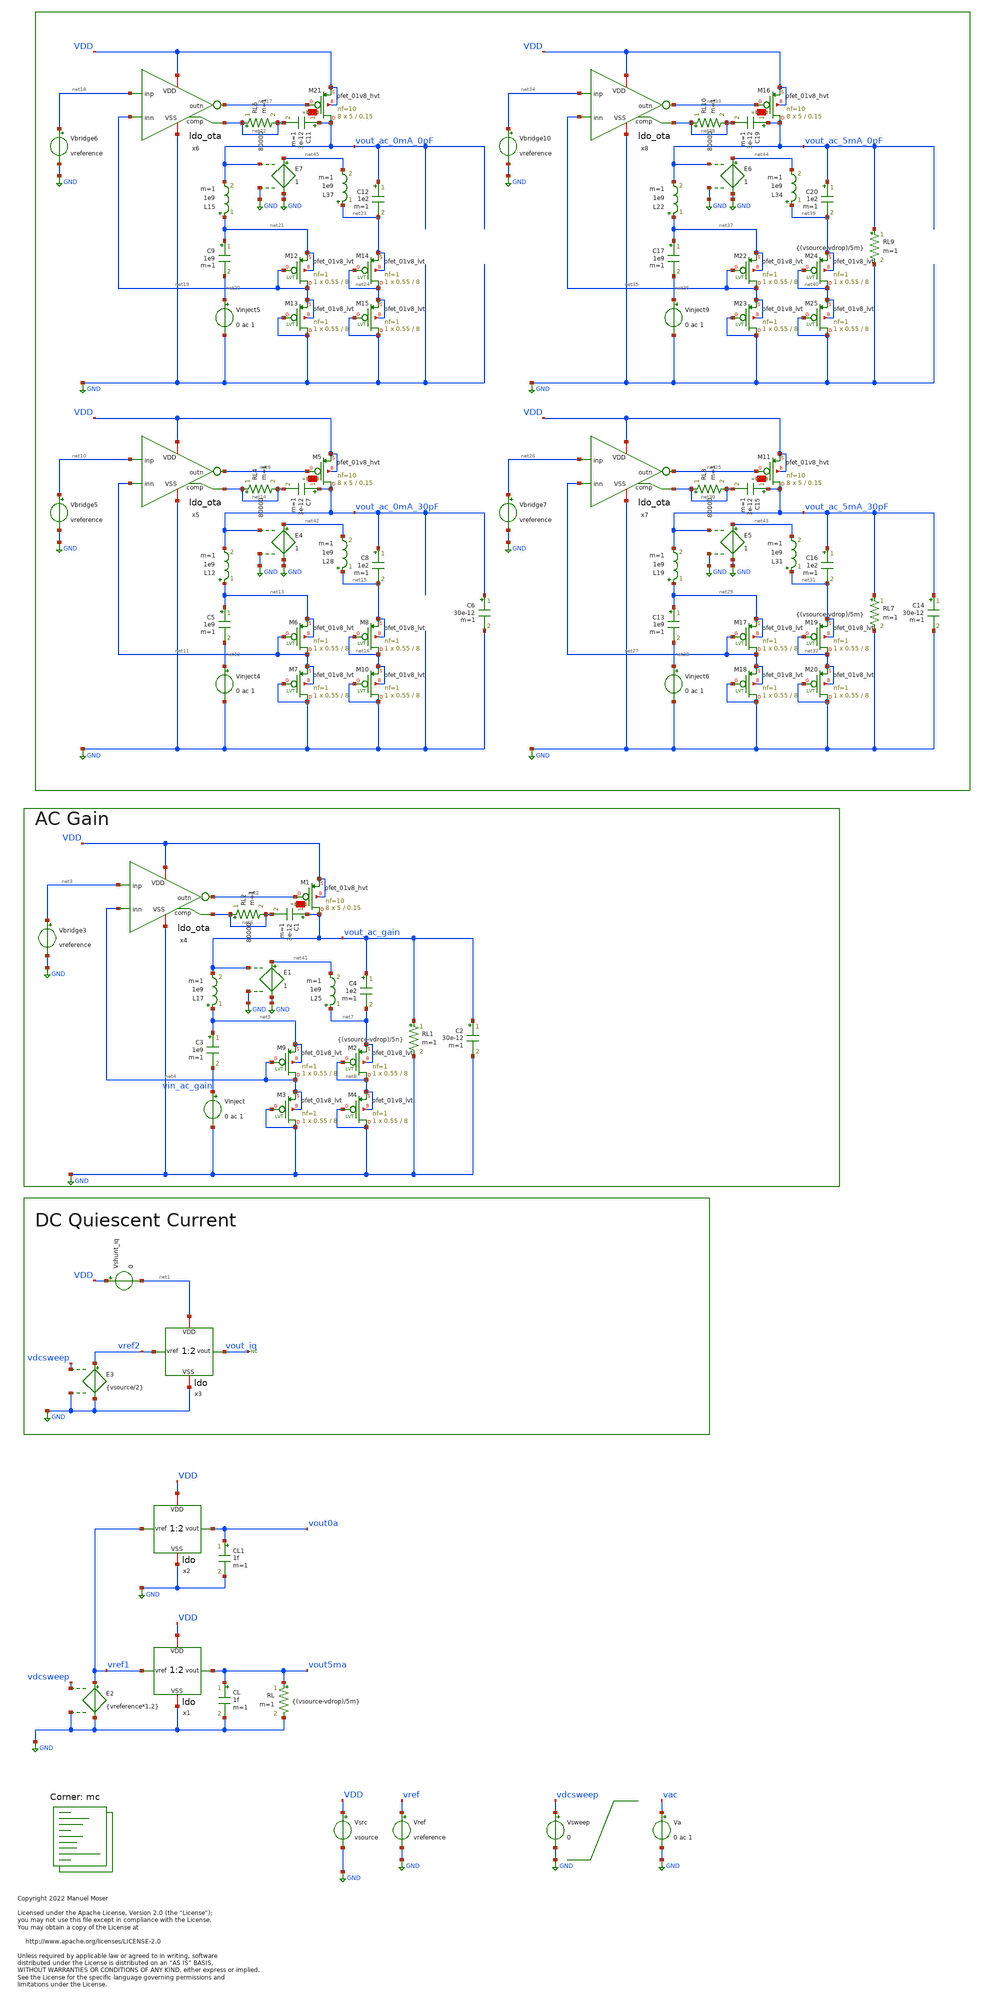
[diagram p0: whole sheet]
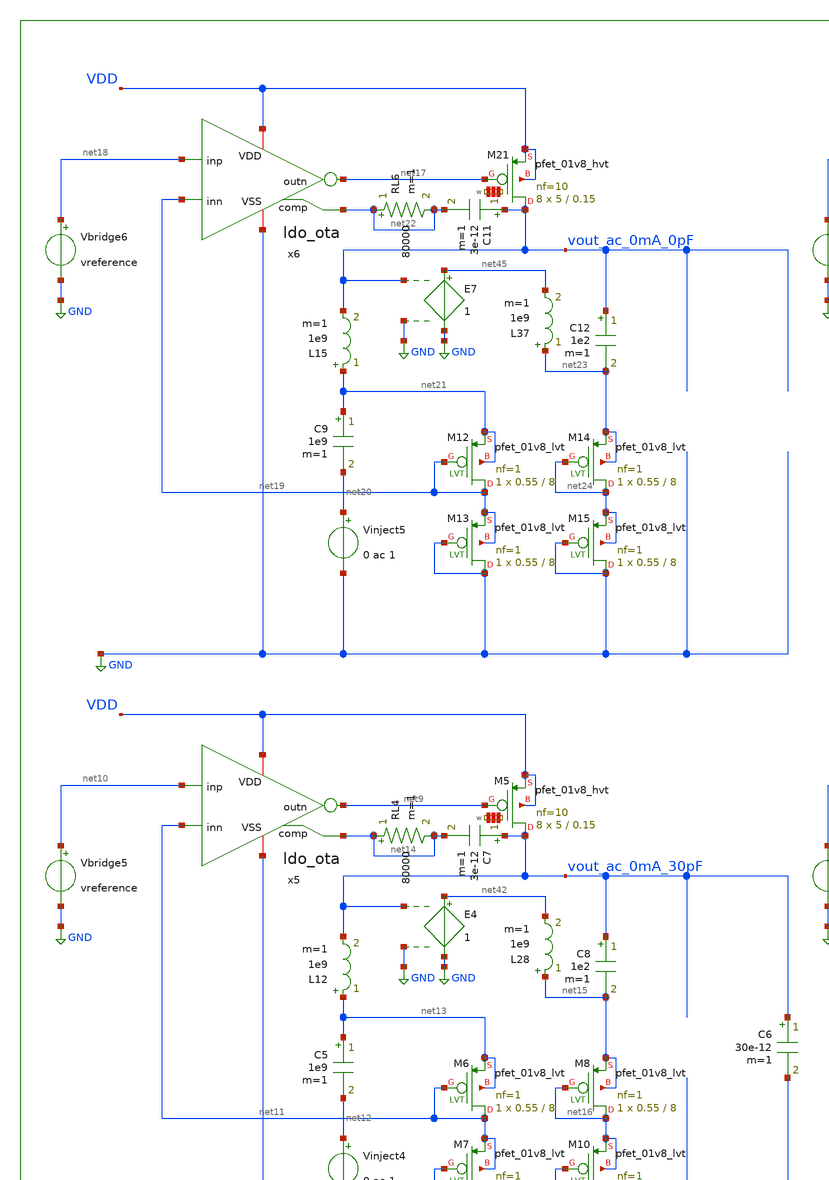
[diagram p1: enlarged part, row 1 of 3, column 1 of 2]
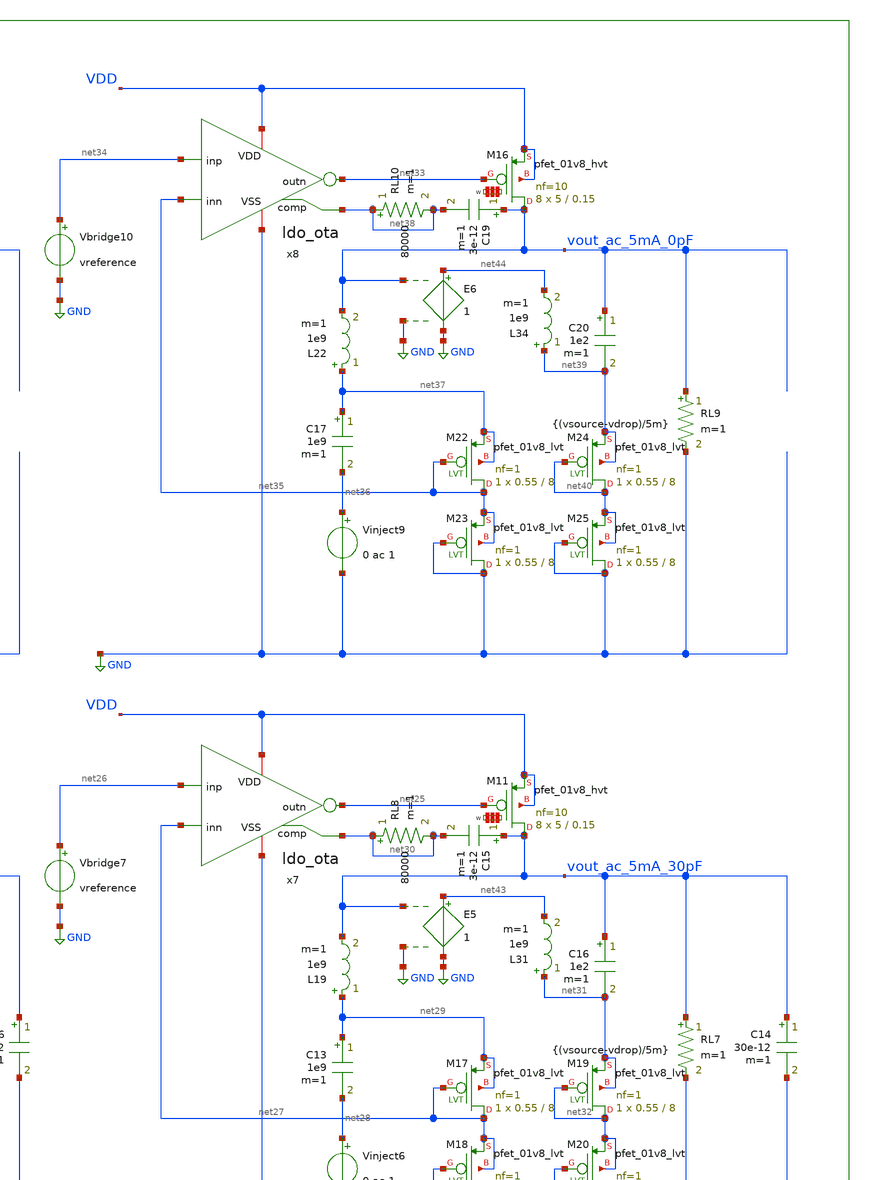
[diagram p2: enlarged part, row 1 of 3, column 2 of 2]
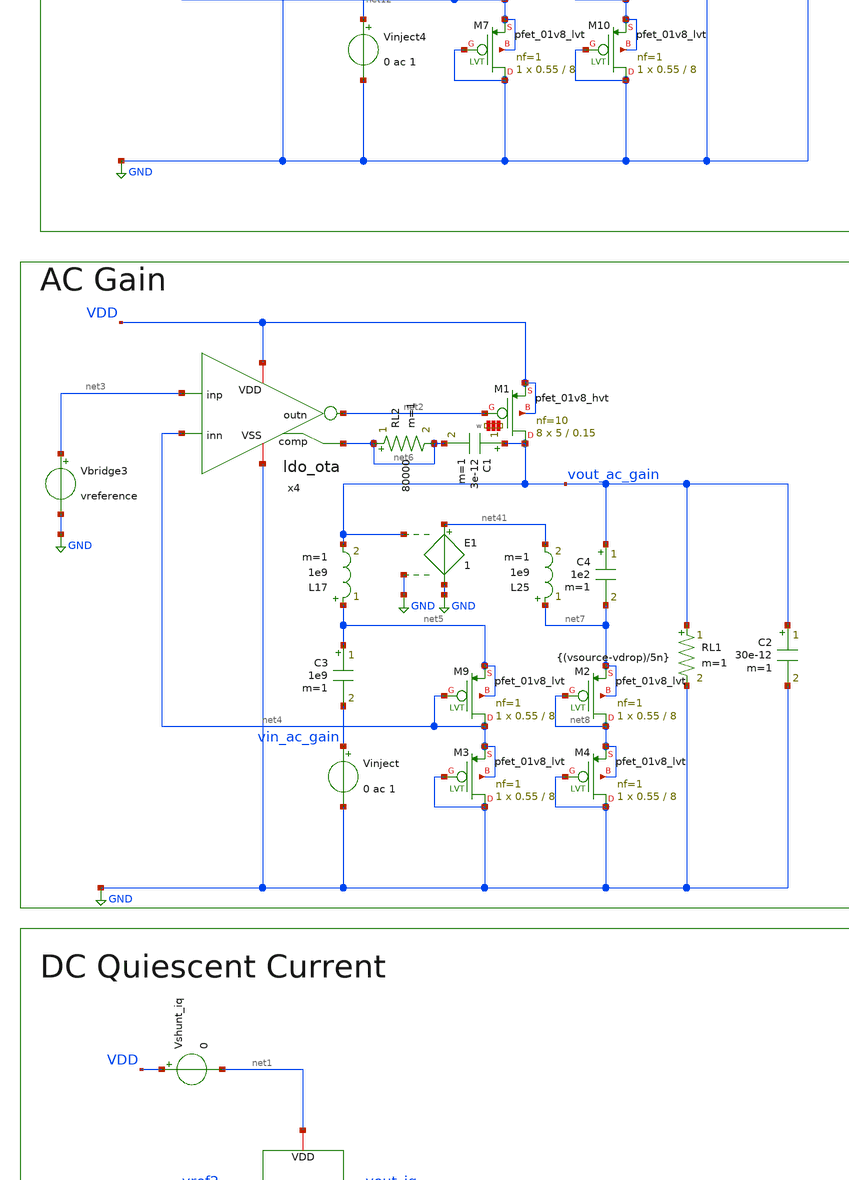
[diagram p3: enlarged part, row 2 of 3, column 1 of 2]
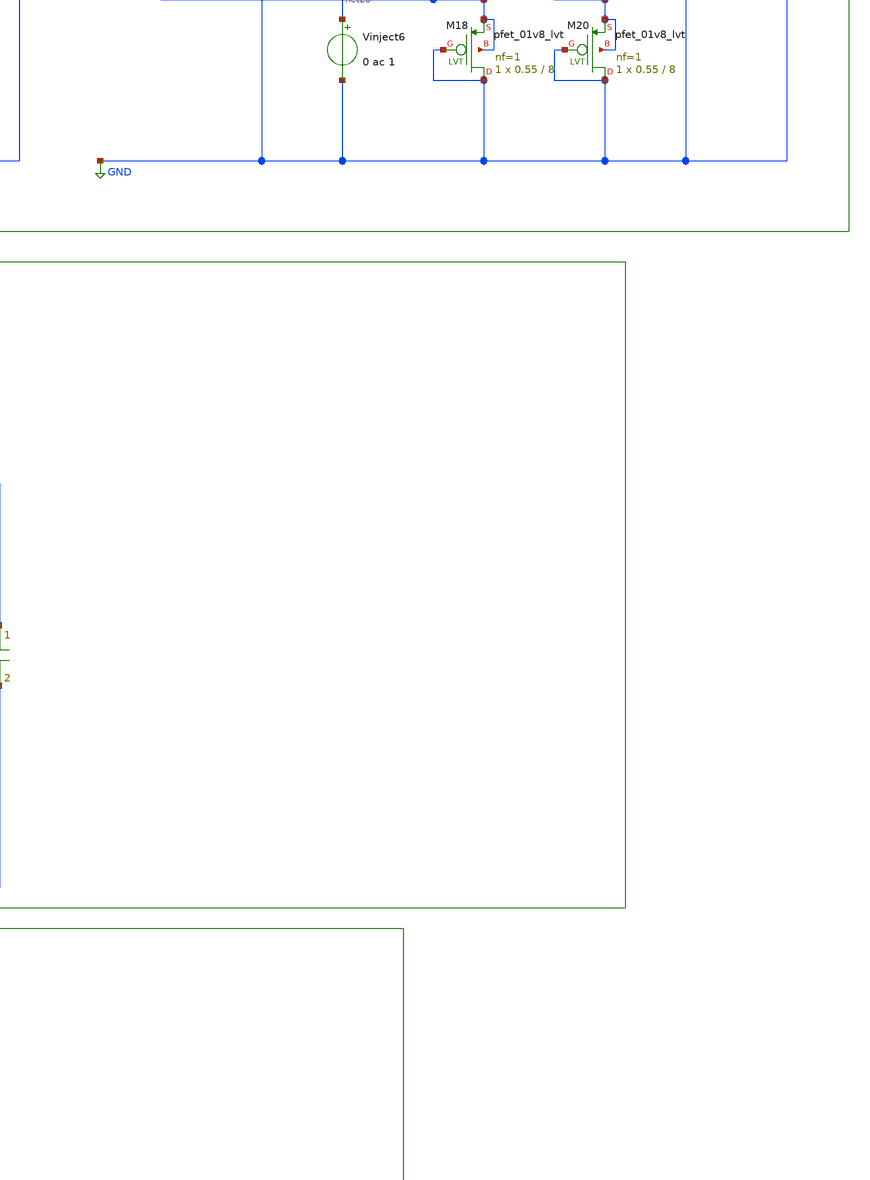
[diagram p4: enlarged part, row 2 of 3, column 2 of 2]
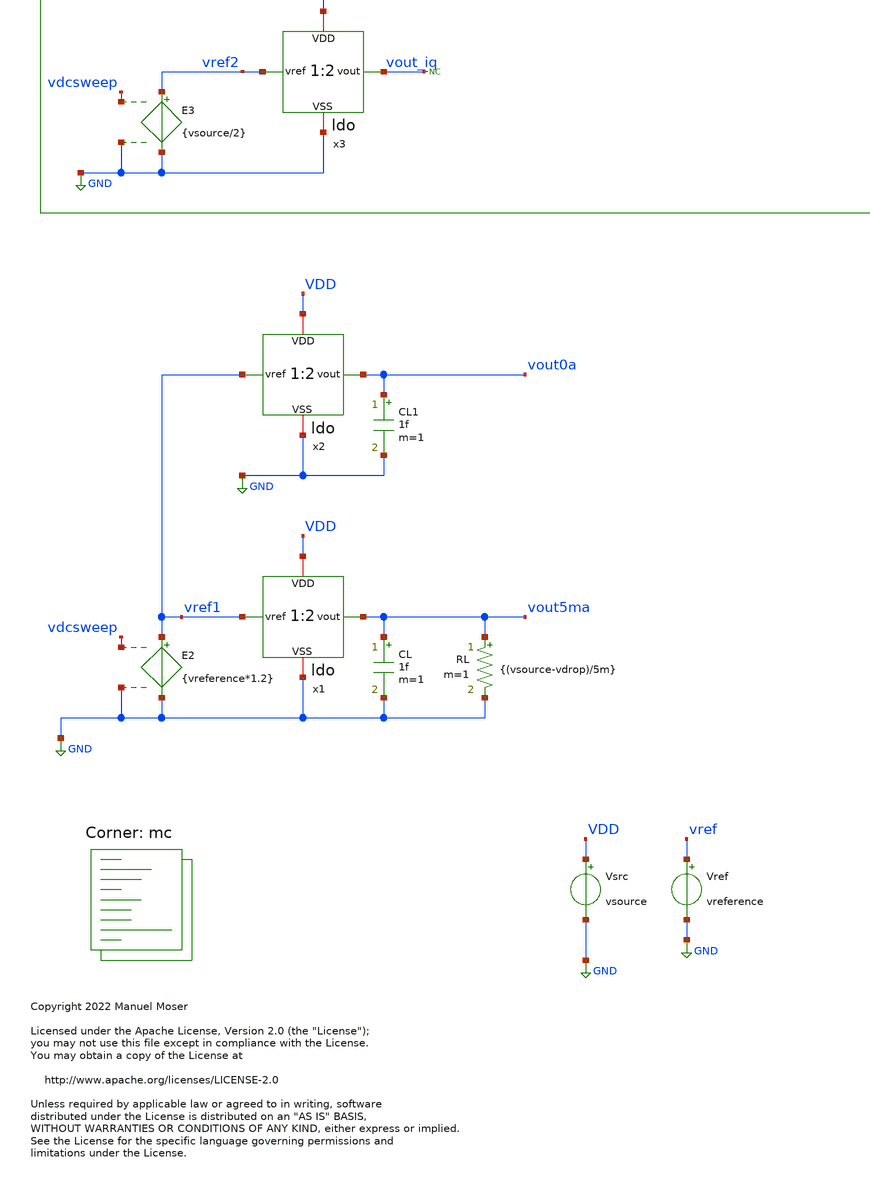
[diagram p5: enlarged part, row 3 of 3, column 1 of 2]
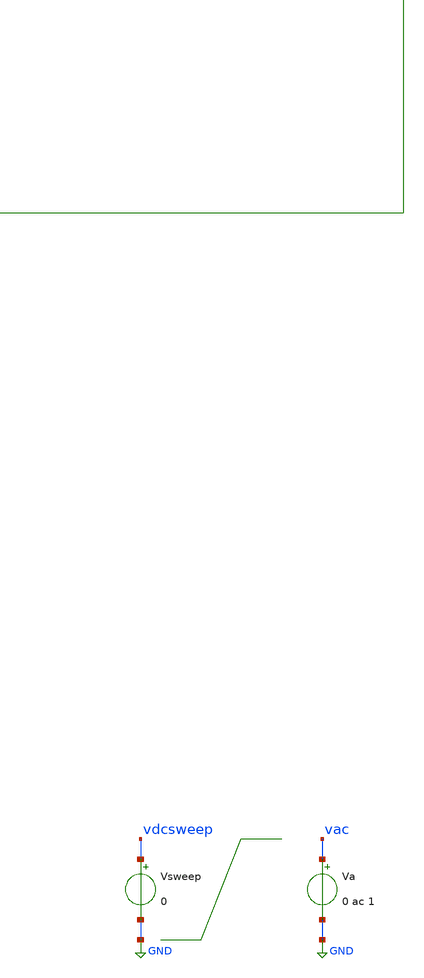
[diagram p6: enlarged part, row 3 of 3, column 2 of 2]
** sch_path: xschem/ldo_tb.sch
* Copyright 2022 Manuel Moser
* Licensed under the Apache License, Version 2.0 (the "License");
**.subckt ldo_tb
Vref vref GND vreference
Vsrc VDD GND vsource
Va vac GND 0 ac 1
CL vout5ma GND 1f m=1
RL vout5ma GND {(vsource-vdrop)/5m} m=1
x1 VDD vref1 vout5ma GND ldo
CL1 vout0a GND 1f m=1
x2 VDD vref1 vout0a GND ldo
Vsweep vdcsweep GND 0
E2 vref1 GND vdcsweep GND {vreference*1.2}
x3 net1 vref2 vout_iq GND ldo
Vshunt_iq VDD net1 0
E3 vref2 GND vdcsweep GND {vsource/2}
* noconn vout_iq
x4 VDD net3 net2 net4 GND net6 ldo_ota
L17 net5 vout_ac_gain 1e9 m=1
C3 net5 vin_ac_gain 1e9 m=1
Vinject vin_ac_gain GND 0 ac 1
Vbridge3 net3 GND vreference
RL1 vout_ac_gain GND {(vsource-vdrop)/5n} m=1
C2 vout_ac_gain GND 30e-12 m=1
C1 vout_ac_gain net6 3e-12 m=1
RL2 net6 net6 80000 m=1
XM9 net4 net4 net5 net5 sky130_fd_pr__pfet_01v8_lvt L=8 W=0.55 nf=1 ad='int((nf+1)/2) * W/nf * 0.29'
+ as='int((nf+2)/2) * W/nf * 0.29' pd='2*int((nf+1)/2) * (W/nf + 0.29)' ps='2*int((nf+2)/2) * (W/nf + 0.29)'
+ nrd='0.29 / W' nrs='0.29 / W' sa=0 sb=0 sd=0 mult=1 m=1
XM3 GND GND net4 net4 sky130_fd_pr__pfet_01v8_lvt L=8 W=0.55 nf=1 ad='int((nf+1)/2) * W/nf * 0.29' as='int((nf+2)/2) * W/nf * 0.29'
+ pd='2*int((nf+1)/2) * (W/nf + 0.29)' ps='2*int((nf+2)/2) * (W/nf + 0.29)' nrd='0.29 / W' nrs='0.29 / W'
+ sa=0 sb=0 sd=0 mult=1 m=1
XM2 net8 net8 net7 net7 sky130_fd_pr__pfet_01v8_lvt L=8 W=0.55 nf=1 ad='int((nf+1)/2) * W/nf * 0.29'
+ as='int((nf+2)/2) * W/nf * 0.29' pd='2*int((nf+1)/2) * (W/nf + 0.29)' ps='2*int((nf+2)/2) * (W/nf + 0.29)'
+ nrd='0.29 / W' nrs='0.29 / W' sa=0 sb=0 sd=0 mult=1 m=1
XM4 GND GND net8 net8 sky130_fd_pr__pfet_01v8_lvt L=8 W=0.55 nf=1 ad='int((nf+1)/2) * W/nf * 0.29' as='int((nf+2)/2) * W/nf * 0.29'
+ pd='2*int((nf+1)/2) * (W/nf + 0.29)' ps='2*int((nf+2)/2) * (W/nf + 0.29)' nrd='0.29 / W' nrs='0.29 / W'
+ sa=0 sb=0 sd=0 mult=1 m=1
C4 vout_ac_gain net7 1e2 m=1
x5 VDD net10 net9 net11 GND net14 ldo_ota
L12 net13 vout_ac_0mA_30pF 1e9 m=1
C5 net13 net12 1e9 m=1
Vinject4 net12 GND 0 ac 1
Vbridge5 net10 GND vreference
C6 vout_ac_0mA_30pF GND 30e-12 m=1
C7 vout_ac_0mA_30pF net14 3e-12 m=1
RL4 net14 net14 80000 m=1
XM6 net11 net11 net13 net13 sky130_fd_pr__pfet_01v8_lvt L=8 W=0.55 nf=1 ad='int((nf+1)/2) * W/nf * 0.29'
+ as='int((nf+2)/2) * W/nf * 0.29' pd='2*int((nf+1)/2) * (W/nf + 0.29)' ps='2*int((nf+2)/2) * (W/nf + 0.29)'
+ nrd='0.29 / W' nrs='0.29 / W' sa=0 sb=0 sd=0 mult=1 m=1
XM7 GND GND net11 net11 sky130_fd_pr__pfet_01v8_lvt L=8 W=0.55 nf=1 ad='int((nf+1)/2) * W/nf * 0.29'
+ as='int((nf+2)/2) * W/nf * 0.29' pd='2*int((nf+1)/2) * (W/nf + 0.29)' ps='2*int((nf+2)/2) * (W/nf + 0.29)'
+ nrd='0.29 / W' nrs='0.29 / W' sa=0 sb=0 sd=0 mult=1 m=1
XM8 net16 net16 net15 net15 sky130_fd_pr__pfet_01v8_lvt L=8 W=0.55 nf=1 ad='int((nf+1)/2) * W/nf * 0.29'
+ as='int((nf+2)/2) * W/nf * 0.29' pd='2*int((nf+1)/2) * (W/nf + 0.29)' ps='2*int((nf+2)/2) * (W/nf + 0.29)'
+ nrd='0.29 / W' nrs='0.29 / W' sa=0 sb=0 sd=0 mult=1 m=1
XM10 GND GND net16 net16 sky130_fd_pr__pfet_01v8_lvt L=8 W=0.55 nf=1 ad='int((nf+1)/2) * W/nf * 0.29'
+ as='int((nf+2)/2) * W/nf * 0.29' pd='2*int((nf+1)/2) * (W/nf + 0.29)' ps='2*int((nf+2)/2) * (W/nf + 0.29)'
+ nrd='0.29 / W' nrs='0.29 / W' sa=0 sb=0 sd=0 mult=1 m=1
C8 vout_ac_0mA_30pF net15 1e2 m=1
x6 VDD net18 net17 net19 GND net22 ldo_ota
L15 net21 vout_ac_0mA_0pF 1e9 m=1
C9 net21 net20 1e9 m=1
Vinject5 net20 GND 0 ac 1
Vbridge6 net18 GND vreference
C11 vout_ac_0mA_0pF net22 3e-12 m=1
RL6 net22 net22 80000 m=1
XM12 net19 net19 net21 net21 sky130_fd_pr__pfet_01v8_lvt L=8 W=0.55 nf=1 ad='int((nf+1)/2) * W/nf * 0.29'
+ as='int((nf+2)/2) * W/nf * 0.29' pd='2*int((nf+1)/2) * (W/nf + 0.29)' ps='2*int((nf+2)/2) * (W/nf + 0.29)'
+ nrd='0.29 / W' nrs='0.29 / W' sa=0 sb=0 sd=0 mult=1 m=1
XM13 GND GND net19 net19 sky130_fd_pr__pfet_01v8_lvt L=8 W=0.55 nf=1 ad='int((nf+1)/2) * W/nf * 0.29'
+ as='int((nf+2)/2) * W/nf * 0.29' pd='2*int((nf+1)/2) * (W/nf + 0.29)' ps='2*int((nf+2)/2) * (W/nf + 0.29)'
+ nrd='0.29 / W' nrs='0.29 / W' sa=0 sb=0 sd=0 mult=1 m=1
XM14 net24 net24 net23 net23 sky130_fd_pr__pfet_01v8_lvt L=8 W=0.55 nf=1 ad='int((nf+1)/2) * W/nf * 0.29'
+ as='int((nf+2)/2) * W/nf * 0.29' pd='2*int((nf+1)/2) * (W/nf + 0.29)' ps='2*int((nf+2)/2) * (W/nf + 0.29)'
+ nrd='0.29 / W' nrs='0.29 / W' sa=0 sb=0 sd=0 mult=1 m=1
XM15 GND GND net24 net24 sky130_fd_pr__pfet_01v8_lvt L=8 W=0.55 nf=1 ad='int((nf+1)/2) * W/nf * 0.29'
+ as='int((nf+2)/2) * W/nf * 0.29' pd='2*int((nf+1)/2) * (W/nf + 0.29)' ps='2*int((nf+2)/2) * (W/nf + 0.29)'
+ nrd='0.29 / W' nrs='0.29 / W' sa=0 sb=0 sd=0 mult=1 m=1
C12 vout_ac_0mA_0pF net23 1e2 m=1
x7 VDD net26 net25 net27 GND net30 ldo_ota
L19 net29 vout_ac_5mA_30pF 1e9 m=1
C13 net29 net28 1e9 m=1
Vinject6 net28 GND 0 ac 1
Vbridge7 net26 GND vreference
RL7 vout_ac_5mA_30pF GND {(vsource-vdrop)/5m} m=1
C14 vout_ac_5mA_30pF GND 30e-12 m=1
C15 vout_ac_5mA_30pF net30 3e-12 m=1
RL8 net30 net30 80000 m=1
XM17 net27 net27 net29 net29 sky130_fd_pr__pfet_01v8_lvt L=8 W=0.55 nf=1 ad='int((nf+1)/2) * W/nf * 0.29'
+ as='int((nf+2)/2) * W/nf * 0.29' pd='2*int((nf+1)/2) * (W/nf + 0.29)' ps='2*int((nf+2)/2) * (W/nf + 0.29)'
+ nrd='0.29 / W' nrs='0.29 / W' sa=0 sb=0 sd=0 mult=1 m=1
XM18 GND GND net27 net27 sky130_fd_pr__pfet_01v8_lvt L=8 W=0.55 nf=1 ad='int((nf+1)/2) * W/nf * 0.29'
+ as='int((nf+2)/2) * W/nf * 0.29' pd='2*int((nf+1)/2) * (W/nf + 0.29)' ps='2*int((nf+2)/2) * (W/nf + 0.29)'
+ nrd='0.29 / W' nrs='0.29 / W' sa=0 sb=0 sd=0 mult=1 m=1
XM19 net32 net32 net31 net31 sky130_fd_pr__pfet_01v8_lvt L=8 W=0.55 nf=1 ad='int((nf+1)/2) * W/nf * 0.29'
+ as='int((nf+2)/2) * W/nf * 0.29' pd='2*int((nf+1)/2) * (W/nf + 0.29)' ps='2*int((nf+2)/2) * (W/nf + 0.29)'
+ nrd='0.29 / W' nrs='0.29 / W' sa=0 sb=0 sd=0 mult=1 m=1
XM20 GND GND net32 net32 sky130_fd_pr__pfet_01v8_lvt L=8 W=0.55 nf=1 ad='int((nf+1)/2) * W/nf * 0.29'
+ as='int((nf+2)/2) * W/nf * 0.29' pd='2*int((nf+1)/2) * (W/nf + 0.29)' ps='2*int((nf+2)/2) * (W/nf + 0.29)'
+ nrd='0.29 / W' nrs='0.29 / W' sa=0 sb=0 sd=0 mult=1 m=1
C16 vout_ac_5mA_30pF net31 1e2 m=1
x8 VDD net34 net33 net35 GND net38 ldo_ota
L22 net37 vout_ac_5mA_0pF 1e9 m=1
C17 net37 net36 1e9 m=1
Vinject9 net36 GND 0 ac 1
Vbridge10 net34 GND vreference
RL9 vout_ac_5mA_0pF GND {(vsource-vdrop)/5m} m=1
C19 vout_ac_5mA_0pF net38 3e-12 m=1
RL10 net38 net38 80000 m=1
XM22 net35 net35 net37 net37 sky130_fd_pr__pfet_01v8_lvt L=8 W=0.55 nf=1 ad='int((nf+1)/2) * W/nf * 0.29'
+ as='int((nf+2)/2) * W/nf * 0.29' pd='2*int((nf+1)/2) * (W/nf + 0.29)' ps='2*int((nf+2)/2) * (W/nf + 0.29)'
+ nrd='0.29 / W' nrs='0.29 / W' sa=0 sb=0 sd=0 mult=1 m=1
XM23 GND GND net35 net35 sky130_fd_pr__pfet_01v8_lvt L=8 W=0.55 nf=1 ad='int((nf+1)/2) * W/nf * 0.29'
+ as='int((nf+2)/2) * W/nf * 0.29' pd='2*int((nf+1)/2) * (W/nf + 0.29)' ps='2*int((nf+2)/2) * (W/nf + 0.29)'
+ nrd='0.29 / W' nrs='0.29 / W' sa=0 sb=0 sd=0 mult=1 m=1
XM24 net40 net40 net39 net39 sky130_fd_pr__pfet_01v8_lvt L=8 W=0.55 nf=1 ad='int((nf+1)/2) * W/nf * 0.29'
+ as='int((nf+2)/2) * W/nf * 0.29' pd='2*int((nf+1)/2) * (W/nf + 0.29)' ps='2*int((nf+2)/2) * (W/nf + 0.29)'
+ nrd='0.29 / W' nrs='0.29 / W' sa=0 sb=0 sd=0 mult=1 m=1
XM25 GND GND net40 net40 sky130_fd_pr__pfet_01v8_lvt L=8 W=0.55 nf=1 ad='int((nf+1)/2) * W/nf * 0.29'
+ as='int((nf+2)/2) * W/nf * 0.29' pd='2*int((nf+1)/2) * (W/nf + 0.29)' ps='2*int((nf+2)/2) * (W/nf + 0.29)'
+ nrd='0.29 / W' nrs='0.29 / W' sa=0 sb=0 sd=0 mult=1 m=1
C20 vout_ac_5mA_0pF net39 1e2 m=1
L25 net7 net41 1e9 m=1
E1 net41 GND vout_ac_gain GND 1
L28 net15 net42 1e9 m=1
E4 net42 GND vout_ac_0mA_30pF GND 1
L31 net31 net43 1e9 m=1
E5 net43 GND vout_ac_5mA_30pF GND 1
L34 net39 net44 1e9 m=1
E6 net44 GND vout_ac_5mA_0pF GND 1
L37 net23 net45 1e9 m=1
E7 net45 GND vout_ac_0mA_0pF GND 1
XM1 vout_ac_gain net2 VDD VDD sky130_fd_pr__pfet_01v8_hvt L=0.15 W='5 * 10 ' nf=10 ad='int((nf+1)/2) * W / nf * 0.29'
+ as='int((nf+2)/2) * W / nf * 0.29' pd='2*int((nf+1)/2) * (W / nf + 0.29)' ps='2*int((nf+2)/2) * (W / nf + 0.29)'
+ nrd='0.29 / W ' nrs='0.29 / W ' sa=0 sb=0 sd=0 mult=8 m=8
XM5 vout_ac_0mA_30pF net9 VDD VDD sky130_fd_pr__pfet_01v8_hvt L=0.15 W='5 * 10 ' nf=10 ad='int((nf+1)/2) * W / nf * 0.29'
+ as='int((nf+2)/2) * W / nf * 0.29' pd='2*int((nf+1)/2) * (W / nf + 0.29)' ps='2*int((nf+2)/2) * (W / nf + 0.29)'
+ nrd='0.29 / W ' nrs='0.29 / W ' sa=0 sb=0 sd=0 mult=8 m=8
XM11 vout_ac_5mA_30pF net25 VDD VDD sky130_fd_pr__pfet_01v8_hvt L=0.15 W='5 * 10 ' nf=10 ad='int((nf+1)/2) * W / nf * 0.29'
+ as='int((nf+2)/2) * W / nf * 0.29' pd='2*int((nf+1)/2) * (W / nf + 0.29)' ps='2*int((nf+2)/2) * (W / nf + 0.29)'
+ nrd='0.29 / W ' nrs='0.29 / W ' sa=0 sb=0 sd=0 mult=8 m=8
XM16 vout_ac_5mA_0pF net33 VDD VDD sky130_fd_pr__pfet_01v8_hvt L=0.15 W='5 * 10 ' nf=10 ad='int((nf+1)/2) * W / nf * 0.29'
+ as='int((nf+2)/2) * W / nf * 0.29' pd='2*int((nf+1)/2) * (W / nf + 0.29)' ps='2*int((nf+2)/2) * (W / nf + 0.29)'
+ nrd='0.29 / W ' nrs='0.29 / W ' sa=0 sb=0 sd=0 mult=8 m=8
XM21 vout_ac_0mA_0pF net17 VDD VDD sky130_fd_pr__pfet_01v8_hvt L=0.15 W='5 * 10 ' nf=10 ad='int((nf+1)/2) * W / nf * 0.29'
+ as='int((nf+2)/2) * W / nf * 0.29' pd='2*int((nf+1)/2) * (W / nf + 0.29)' ps='2*int((nf+2)/2) * (W / nf + 0.29)'
+ nrd='0.29 / W ' nrs='0.29 / W ' sa=0 sb=0 sd=0 mult=8 m=8
**** begin user architecture code



.temp 27
*.option gmin = 1e-16
.option RSHUNT=1E15
.option method = gear

.param vsource = 1.80
.param vdrop = 0.20
.param vreference = {(vsource-vdrop)/2}

.save all
.options savecurrents

.control
set num_threads = 12
write results_ldo.raw
set appendwrite

repeat 10
reset

dc vsweep 0 1 0.01 temp -30 60 90
*dc vsweep 0 1 0.01
write results_ldo.raw   vref1 vout5ma vout0a x1.vota x1.vfb
+ @m.x1.xm9.msky130_fd_pr__pfet_01v8_lvt[id]  vref2 i(vshunt_iq) vout_ac_gain

ac dec 10 1 10meg
write results_ldo.raw vout_ac_0mA_0pF vout_ac_0mA_30pF vout_ac_5mA_0pF vout_ac_5mA_30pF

*pz vinject gnd vout_ac_gain gnd vol pz


end

.endc




.lib $::SKYWATER_MODELS/sky130.lib.spice mc
**** end user architecture code
**.ends
.GLOBAL GND
.end
